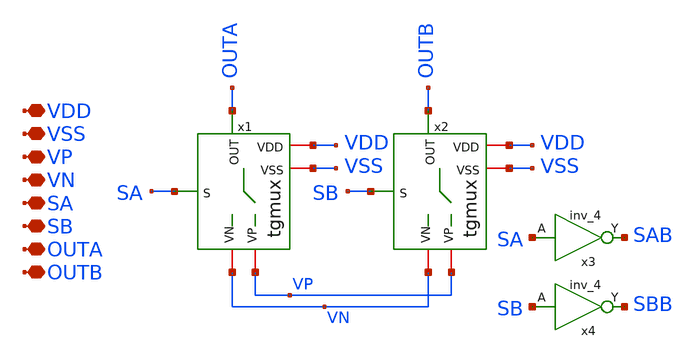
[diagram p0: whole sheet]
** sch_path: xschem/sar-adc/tgmuxdiff.sch
**.subckt tgmuxdiff VDD VSS VP VN SA OUTA OUTB SB
*.iopin VDD
*.iopin VSS
*.iopin VP
*.iopin VN
*.iopin SA
*.iopin OUTA
*.iopin OUTB
*.iopin SB
x1 VP VN SA OUTA VDD VSS tgmux
x2 VP VN SB OUTB VDD VSS tgmux
x3 SA VGND VNB VPB VPWR SAB sky130_fd_sc_hd__inv_4
x4 SB VGND VNB VPB VPWR SBB sky130_fd_sc_hd__inv_4
**.ends

* expanding   symbol:  tgmux.sym # of pins=6
** sym_path: xschem/sar-adc/tgmux.sym
** sch_path: xschem/sar-adc/tgmux.sch
.subckt tgmux VP VN S OUT VDD VSS
*.iopin VP
*.iopin VN
*.ipin S
*.opin OUT
*.iopin VDD
*.iopin VSS
XM1 OUT SB VN VSS sky130_fd_pr__nfet_01v8 L=0.15 W=2.5 nf=1 ad='int((1 + 1)/2) * 2.5 / 1 * 0.29' as='int((1 + 2)/2) * 2.5 / 1 * 0.29'
+ pd='2*int((1 + 1)/2) * (2.5 / 1 + 0.29)' ps='2*int((1 + 2)/2) * (2.5 / 1 + 0.29)' nrd='0.29 / 2.5 ' nrs='0.29 / 2.5 '
+ sa=0 sb=0 sd=0 mult=1 m=1
XM2 OUT S VN VDD sky130_fd_pr__pfet_01v8 L=0.15 W=5 nf=1 ad='int((1 + 1)/2) * 5 / 1 * 0.29' as='int((1 + 2)/2) * 5 / 1 * 0.29'
+ pd='2*int((1 + 1)/2) * (5 / 1 + 0.29)' ps='2*int((1 + 2)/2) * (5 / 1 + 0.29)' nrd='0.29 / 5 ' nrs='0.29 / 5 '
+ sa=0 sb=0 sd=0 mult=1 m=1
XM3 OUT S VP VSS sky130_fd_pr__nfet_01v8 L=0.15 W=2.5 nf=1 ad='int((1 + 1)/2) * 2.5 / 1 * 0.29' as='int((1 + 2)/2) * 2.5 / 1 * 0.29'
+ pd='2*int((1 + 1)/2) * (2.5 / 1 + 0.29)' ps='2*int((1 + 2)/2) * (2.5 / 1 + 0.29)' nrd='0.29 / 2.5 ' nrs='0.29 / 2.5 '
+ sa=0 sb=0 sd=0 mult=1 m=1
XM4 OUT SB VP VDD sky130_fd_pr__pfet_01v8 L=0.15 W=5 nf=1 ad='int((1 + 1)/2) * 5 / 1 * 0.29' as='int((1 + 2)/2) * 5 / 1 * 0.29'
+ pd='2*int((1 + 1)/2) * (5 / 1 + 0.29)' ps='2*int((1 + 2)/2) * (5 / 1 + 0.29)' nrd='0.29 / 5 ' nrs='0.29 / 5 '
+ sa=0 sb=0 sd=0 mult=1 m=1
x1 S VSS VSS VDD VDD SB sky130_fd_sc_hd__inv_4
.ends

.end
